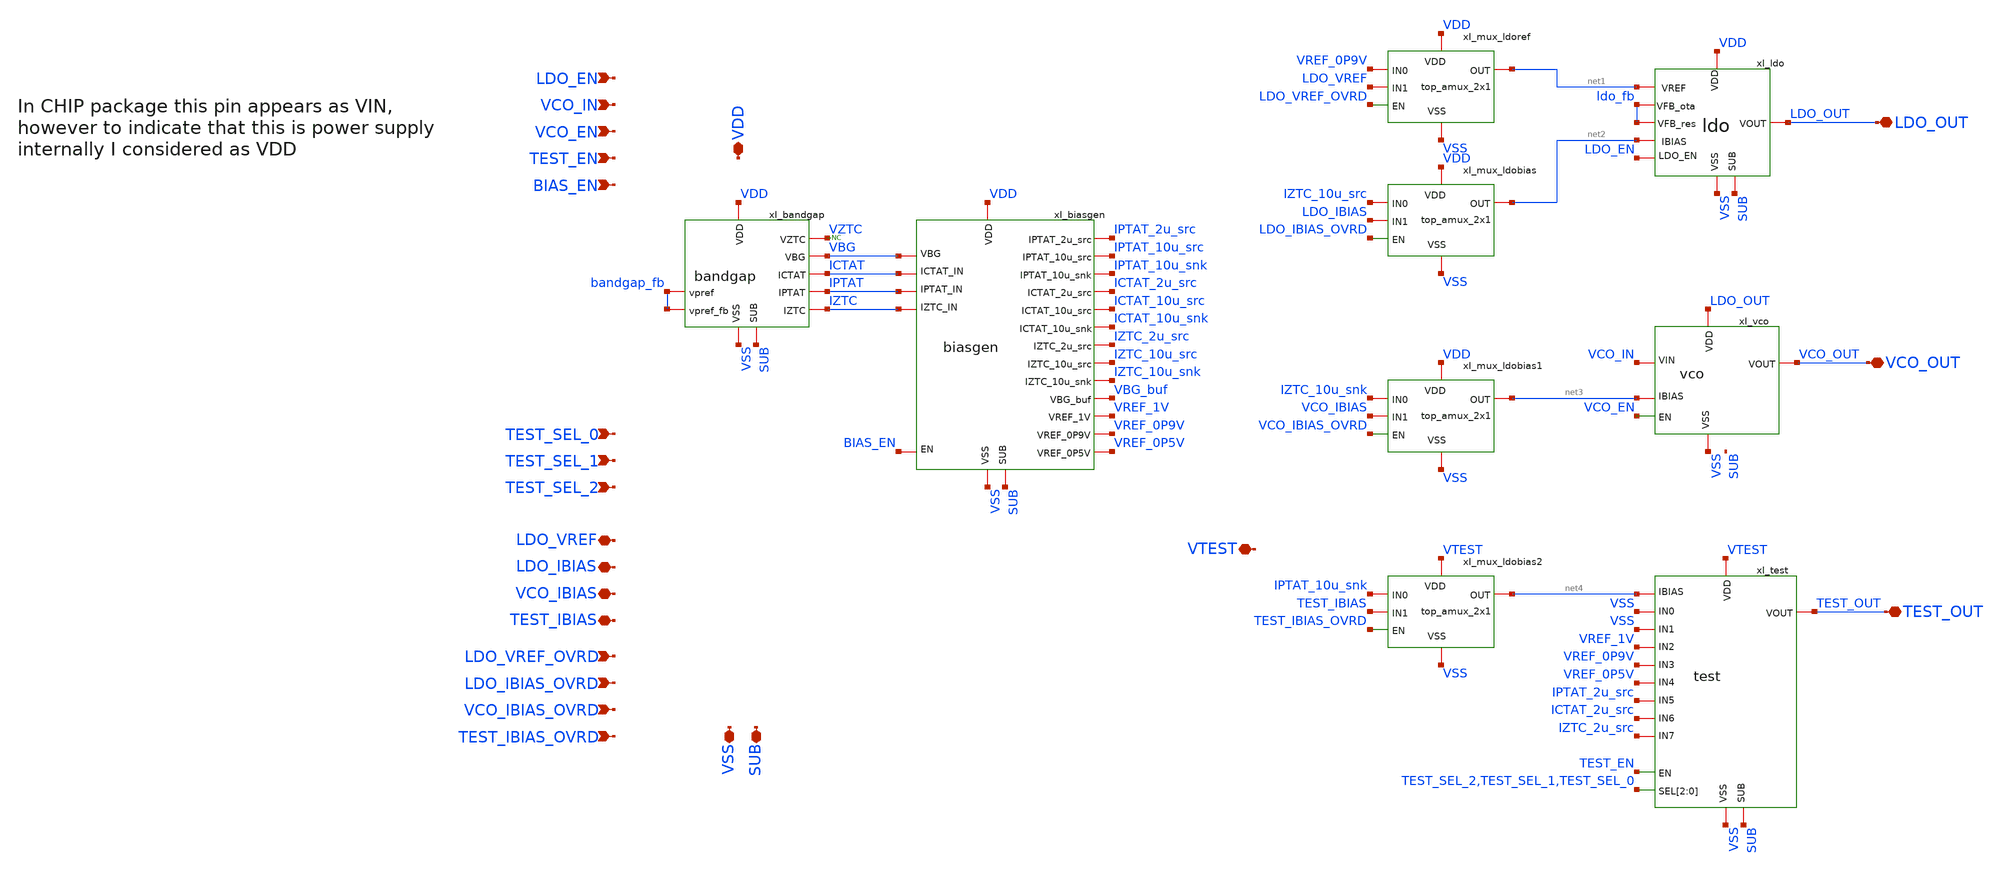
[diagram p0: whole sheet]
** sch_path: designs/libs/A1_core/A1_top_core/top.sch
**.subckt top TEST_SEL_0 VCO_IN VDD VSS SUB LDO_OUT VCO_OUT TEST_OUT TEST_EN VCO_EN TEST_SEL_1
*+ TEST_SEL_2 LDO_VREF LDO_IBIAS VCO_IBIAS TEST_IBIAS LDO_VREF_OVRD LDO_IBIAS_OVRD VCO_IBIAS_OVRD TEST_IBIAS_OVRD
*+ BIAS_EN LDO_EN VTEST
*.ipin TEST_SEL_0
*.ipin VCO_IN
*.iopin VDD
*.iopin VSS
*.iopin SUB
*.iopin LDO_OUT
*.iopin VCO_OUT
*.iopin TEST_OUT
*.ipin TEST_EN
*.ipin VCO_EN
*.ipin TEST_SEL_1
*.ipin TEST_SEL_2
*.iopin LDO_VREF
*.iopin LDO_IBIAS
*.iopin VCO_IBIAS
*.iopin TEST_IBIAS
*.ipin LDO_VREF_OVRD
*.ipin LDO_IBIAS_OVRD
*.ipin VCO_IBIAS_OVRD
*.ipin TEST_IBIAS_OVRD
*.ipin BIAS_EN
*.ipin LDO_EN
*.iopin VTEST
xI_bandgap VDD VBG IPTAT IZTC SUB VSS bandgap_fb bandgap_fb ICTAT VZTC bandgap
xI_biasgen VDD VBG IPTAT_2u_src IPTAT VREF_1V IZTC VREF_0P5V SUB VSS VREF_0P9V ICTAT IPTAT_10u_src
+ IPTAT_10u_snk ICTAT_2u_src ICTAT_10u_src ICTAT_10u_snk IZTC_2u_src IZTC_10u_src IZTC_10u_snk BIAS_EN VBG_buf
+ biasgen
xI_ldo VDD net1 LDO_OUT net2 SUB VSS LDO_EN ldo_fb ldo_fb ldo
xI_vco LDO_OUT net3 VCO_OUT VCO_EN VSS VCO_IN vco
xI_test VTEST net4 TEST_OUT TEST_EN TEST_SEL_2 TEST_SEL_1 TEST_SEL_0 SUB VSS VSS VSS VREF_1V
+ VREF_0P9V VREF_0P5V IPTAT_2u_src ICTAT_2u_src IZTC_2u_src test
xI_mux_ldoref VREF_0P9V VDD net1 VSS LDO_VREF LDO_VREF_OVRD top_amux_2x1
xI_mux_ldobias IZTC_10u_src VDD net2 VSS LDO_IBIAS LDO_IBIAS_OVRD top_amux_2x1
xI_mux_ldobias1 IZTC_10u_snk VDD net3 VSS VCO_IBIAS VCO_IBIAS_OVRD top_amux_2x1
xI_mux_ldobias2 IPTAT_10u_snk VTEST net4 VSS TEST_IBIAS TEST_IBIAS_OVRD top_amux_2x1
* noconn VZTC
**.ends
.end
